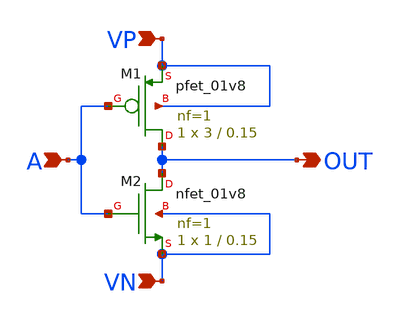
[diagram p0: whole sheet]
** sch_path: basic_cell/single_cell/inverter/inverter.sch
**.subckt inverter A VP VN OUT
*.ipin A
*.ipin VP
*.ipin VN
*.opin OUT
XM1 OUT A VP VP sky130_fd_pr__pfet_01v8 L=0.15 W=3 nf=1 ad='int((nf+1)/2) * W/nf * 0.29' as='int((nf+2)/2) * W/nf * 0.29'
+ pd='2*int((nf+1)/2) * (W/nf + 0.29)' ps='2*int((nf+2)/2) * (W/nf + 0.29)' nrd='0.29 / W' nrs='0.29 / W'
+ sa=0 sb=0 sd=0 mult=1 m=1
XM2 OUT A VN VN sky130_fd_pr__nfet_01v8 L=0.15 W=1 nf=1 ad='int((nf+1)/2) * W/nf * 0.29' as='int((nf+2)/2) * W/nf * 0.29'
+ pd='2*int((nf+1)/2) * (W/nf + 0.29)' ps='2*int((nf+2)/2) * (W/nf + 0.29)' nrd='0.29 / W' nrs='0.29 / W'
+ sa=0 sb=0 sd=0 mult=1 m=1
**.ends
.end
